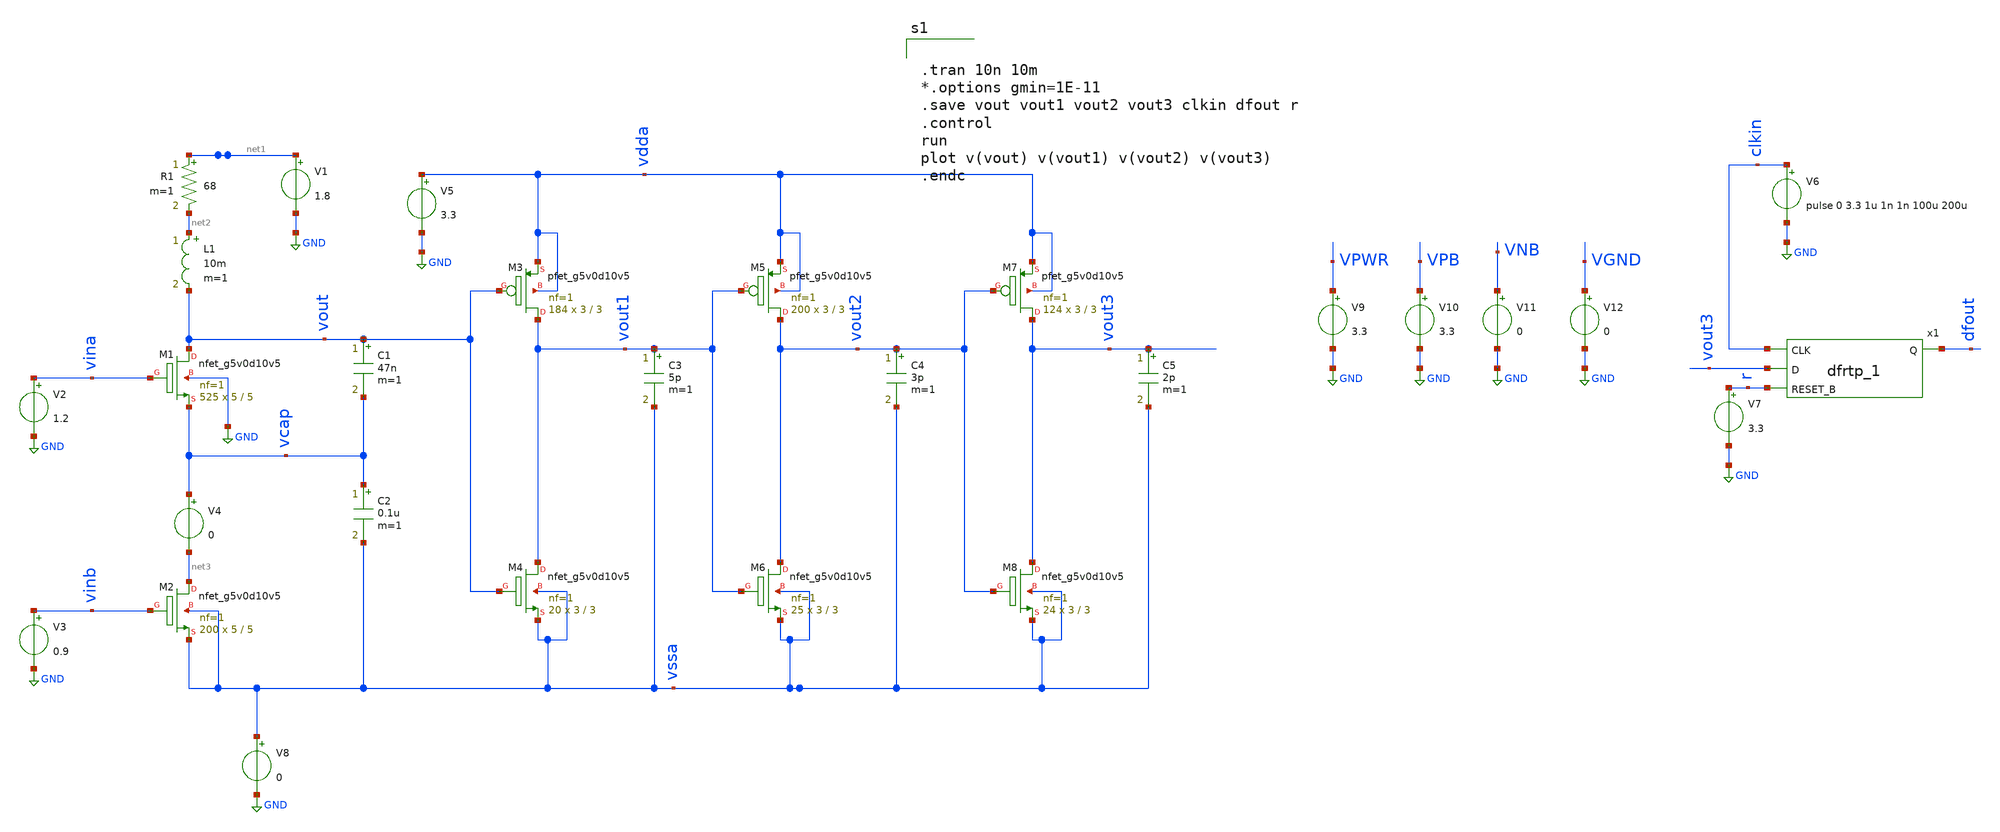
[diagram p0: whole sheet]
** sch_path: xschem/colpitts_slopeamp.sch
**.subckt colpitts_slopeamp
V1 net1 GND 1.8
XM1 vout vina vcap GND sky130_fd_pr__nfet_g5v0d10v5 L=5 W=5 nf=1 ad='int((nf+1)/2) * W/nf * 0.29' as='int((nf+2)/2) * W/nf * 0.29'
+ pd='2*int((nf+1)/2) * (W/nf + 0.29)' ps='2*int((nf+2)/2) * (W/nf + 0.29)' nrd='0.29 / W' nrs='0.29 / W'
+ sa=0 sb=0 sd=0 mult=525 m=525
V2 vina GND 1.2
L1 net2 vout 10m m=1
R1 net1 net2 68 m=1
C1 vout vcap 47n m=1
C2 vcap vssa 0.1u m=1
V4 vcap net3 0
XM2 net3 vinb vssa vssa sky130_fd_pr__nfet_g5v0d10v5 L=5 W=5 nf=1 ad='int((nf+1)/2) * W/nf * 0.29' as='int((nf+2)/2) * W/nf * 0.29'
+ pd='2*int((nf+1)/2) * (W/nf + 0.29)' ps='2*int((nf+2)/2) * (W/nf + 0.29)' nrd='0.29 / W' nrs='0.29 / W'
+ sa=0 sb=0 sd=0 mult=200 m=200
V3 vinb GND 0.9
XM3 vout1 vout vdda vdda sky130_fd_pr__pfet_g5v0d10v5 L=3 W=3 nf=1 ad='int((nf+1)/2) * W/nf * 0.29' as='int((nf+2)/2) * W/nf * 0.29'
+ pd='2*int((nf+1)/2) * (W/nf + 0.29)' ps='2*int((nf+2)/2) * (W/nf + 0.29)' nrd='0.29 / W' nrs='0.29 / W'
+ sa=0 sb=0 sd=0 mult=184 m=184
XM4 vout1 vout vssa vssa sky130_fd_pr__nfet_g5v0d10v5 L=3 W=3 nf=1 ad='int((nf+1)/2) * W/nf * 0.29' as='int((nf+2)/2) * W/nf * 0.29'
+ pd='2*int((nf+1)/2) * (W/nf + 0.29)' ps='2*int((nf+2)/2) * (W/nf + 0.29)' nrd='0.29 / W' nrs='0.29 / W'
+ sa=0 sb=0 sd=0 mult=20 m=20
V5 vdda GND 3.3
C3 vout1 vssa 5p m=1
XM5 vout2 vout1 vdda vdda sky130_fd_pr__pfet_g5v0d10v5 L=3 W=3 nf=1 ad='int((nf+1)/2) * W/nf * 0.29'
+ as='int((nf+2)/2) * W/nf * 0.29' pd='2*int((nf+1)/2) * (W/nf + 0.29)' ps='2*int((nf+2)/2) * (W/nf + 0.29)'
+ nrd='0.29 / W' nrs='0.29 / W' sa=0 sb=0 sd=0 mult=200 m=200
XM6 vout2 vout1 vssa vssa sky130_fd_pr__nfet_g5v0d10v5 L=3 W=3 nf=1 ad='int((nf+1)/2) * W/nf * 0.29'
+ as='int((nf+2)/2) * W/nf * 0.29' pd='2*int((nf+1)/2) * (W/nf + 0.29)' ps='2*int((nf+2)/2) * (W/nf + 0.29)'
+ nrd='0.29 / W' nrs='0.29 / W' sa=0 sb=0 sd=0 mult=25 m=25
C4 vout2 vssa 3p m=1
XM7 vout3 vout2 vdda vdda sky130_fd_pr__pfet_g5v0d10v5 L=3 W=3 nf=1 ad='int((nf+1)/2) * W/nf * 0.29'
+ as='int((nf+2)/2) * W/nf * 0.29' pd='2*int((nf+1)/2) * (W/nf + 0.29)' ps='2*int((nf+2)/2) * (W/nf + 0.29)'
+ nrd='0.29 / W' nrs='0.29 / W' sa=0 sb=0 sd=0 mult=124 m=124
XM8 vout3 vout2 vssa vssa sky130_fd_pr__nfet_g5v0d10v5 L=3 W=3 nf=1 ad='int((nf+1)/2) * W/nf * 0.29'
+ as='int((nf+2)/2) * W/nf * 0.29' pd='2*int((nf+1)/2) * (W/nf + 0.29)' ps='2*int((nf+2)/2) * (W/nf + 0.29)'
+ nrd='0.29 / W' nrs='0.29 / W' sa=0 sb=0 sd=0 mult=24 m=24
C5 vout3 vssa 2p m=1
V6 clkin GND pulse 0 3.3 1u 1n 1n 100u 200u
V7 r GND 3.3
V8 vssa GND 0
x1 clkin vout3 r VGND VNB VPB VPWR dfout sky130_fd_sc_hvl__dfrtp_1
V9 VPWR GND 3.3
V10 VPB GND 3.3
V11 VNB GND 0
V12 VGND GND 0
**** begin user architecture code
  .lib /home/vinodhini/open_pdks/sky130/sky130A/libs.tech/ngspice/sky130.lib.spice tt
.include /home/vinodhini/open_pdks/sky130/sky130A/libs.ref/sky130_fd_sc_hvl/spice/sky130_fd_sc_hvl.spice
.param mc_mm_switch=0
 .param mc_pr_switch=0


.tran 10n 10m
*.options gmin=1E-11
.save vout vout1 vout2 vout3 clkin dfout r
.control
run
plot v(vout) v(vout1) v(vout2) v(vout3)
.endc

**** end user architecture code
**.ends
.GLOBAL GND
.end
